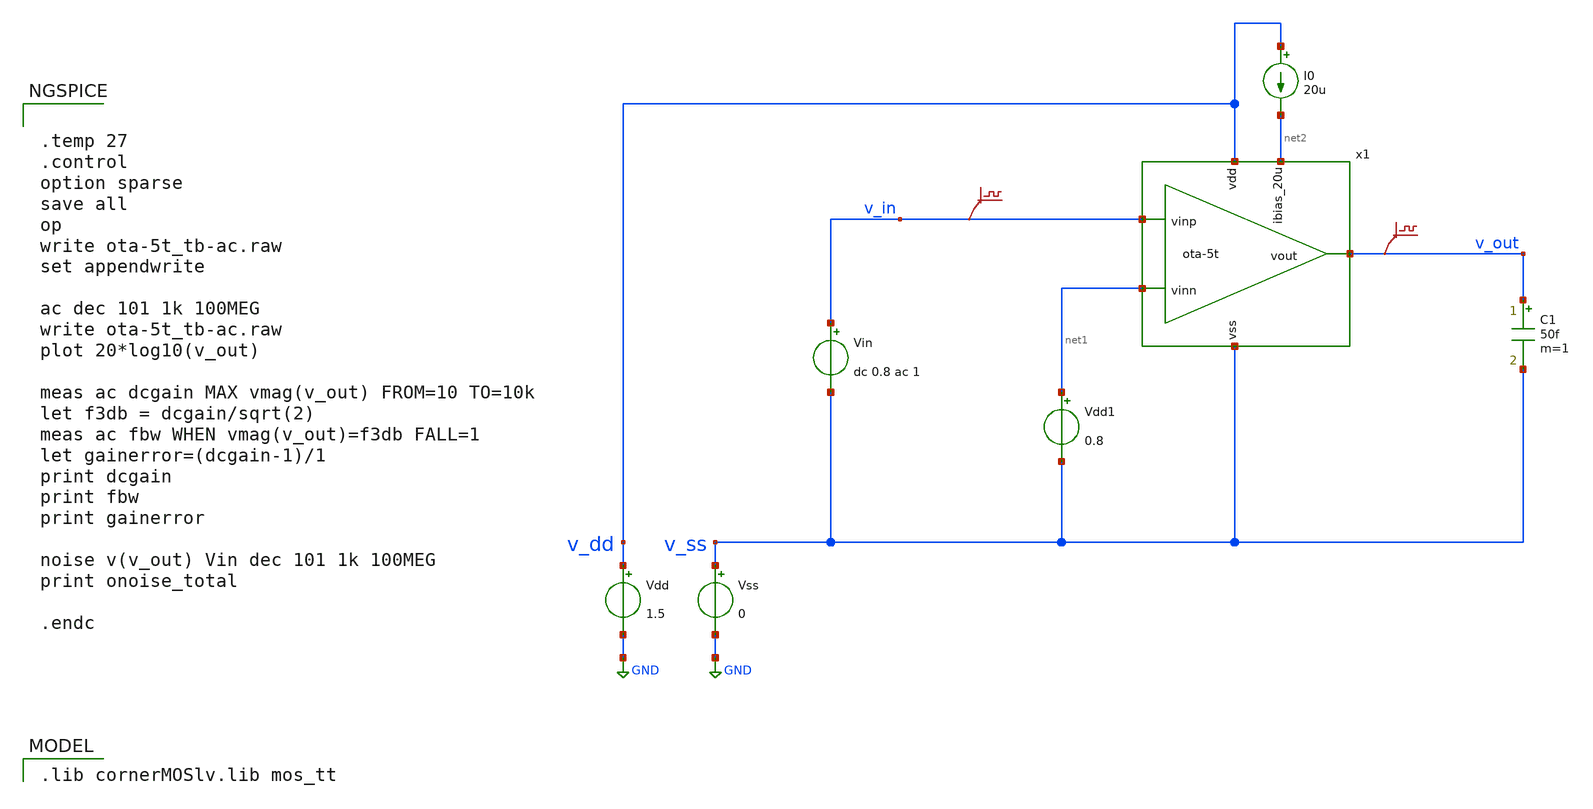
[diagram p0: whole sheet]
** sch_path: Modulo_Analogico/Lab8/ota-5t_tb-ac.sch
* (c) 2024-2025 Harald Pretl, Apache-2.0 license
**.subckt ota-5t_tb-ac
Vdd v_dd GND 1.5
Vss v_ss GND 0
C1 v_out v_ss 50f m=1
Vin v_in v_ss dc 0.8 ac 1
I0 v_dd net2 20u
.save v(v_in)
.save v(v_out)
x1 v_dd v_out v_in net1 net2 v_ss ota-5t
Vdd1 net1 v_ss 0.8
**** begin user architecture code
 .lib cornerMOSlv.lib mos_tt



.temp 27
.control
option sparse
save all
op
write ota-5t_tb-ac.raw
set appendwrite

ac dec 101 1k 100MEG
write ota-5t_tb-ac.raw
plot 20*log10(v_out)

meas ac dcgain MAX vmag(v_out) FROM=10 TO=10k
let f3db = dcgain/sqrt(2)
meas ac fbw WHEN vmag(v_out)=f3db FALL=1
let gainerror=(dcgain-1)/1
print dcgain
print fbw
print gainerror

noise v(v_out) Vin dec 101 1k 100MEG
print onoise_total

.endc


**** end user architecture code
**.ends

* expanding   symbol:  /home/juan/Documents/SEED_Bootcamp_ihp/Modulo_Analogico/Lab8/ota-5t.sym # of
*+ pins=6
** sym_path: Modulo_Analogico/Lab8/ota-5t.sym
** sch_path: Modulo_Analogico/Lab8/ota-5t.sch
.subckt ota-5t vdd vout vinp vinn ibias_20u vss
*.ipin ibias_20u
*.iopin vdd
*.iopin vss
*.ipin vinp
*.ipin vinn
*.opin vout
XM5 tail ibias_20u vss vss sg13_lv_nmos w=0.5u l=5u ng=1 m=1 mm_ok=1
XM4 vout net1 vdd vdd sg13_lv_pmos w=1.5u l=5u ng=1 m=1 mm_ok=1
XM1 net1 vinp tail vss sg13_lv_nmos w=2u l=5u ng=1 m=1 mm_ok=1
XM2 vout vinn tail vss sg13_lv_nmos w=2u l=5u ng=1 m=1 mm_ok=1
XM3 net1 net1 vdd vdd sg13_lv_pmos w=1.5u l=5u ng=1 m=1 mm_ok=1
XM6 ibias_20u ibias_20u vss vss sg13_lv_nmos w=2.5u l=5u ng=5 m=1 mm_ok=1
.ends

.GLOBAL GND
.end
